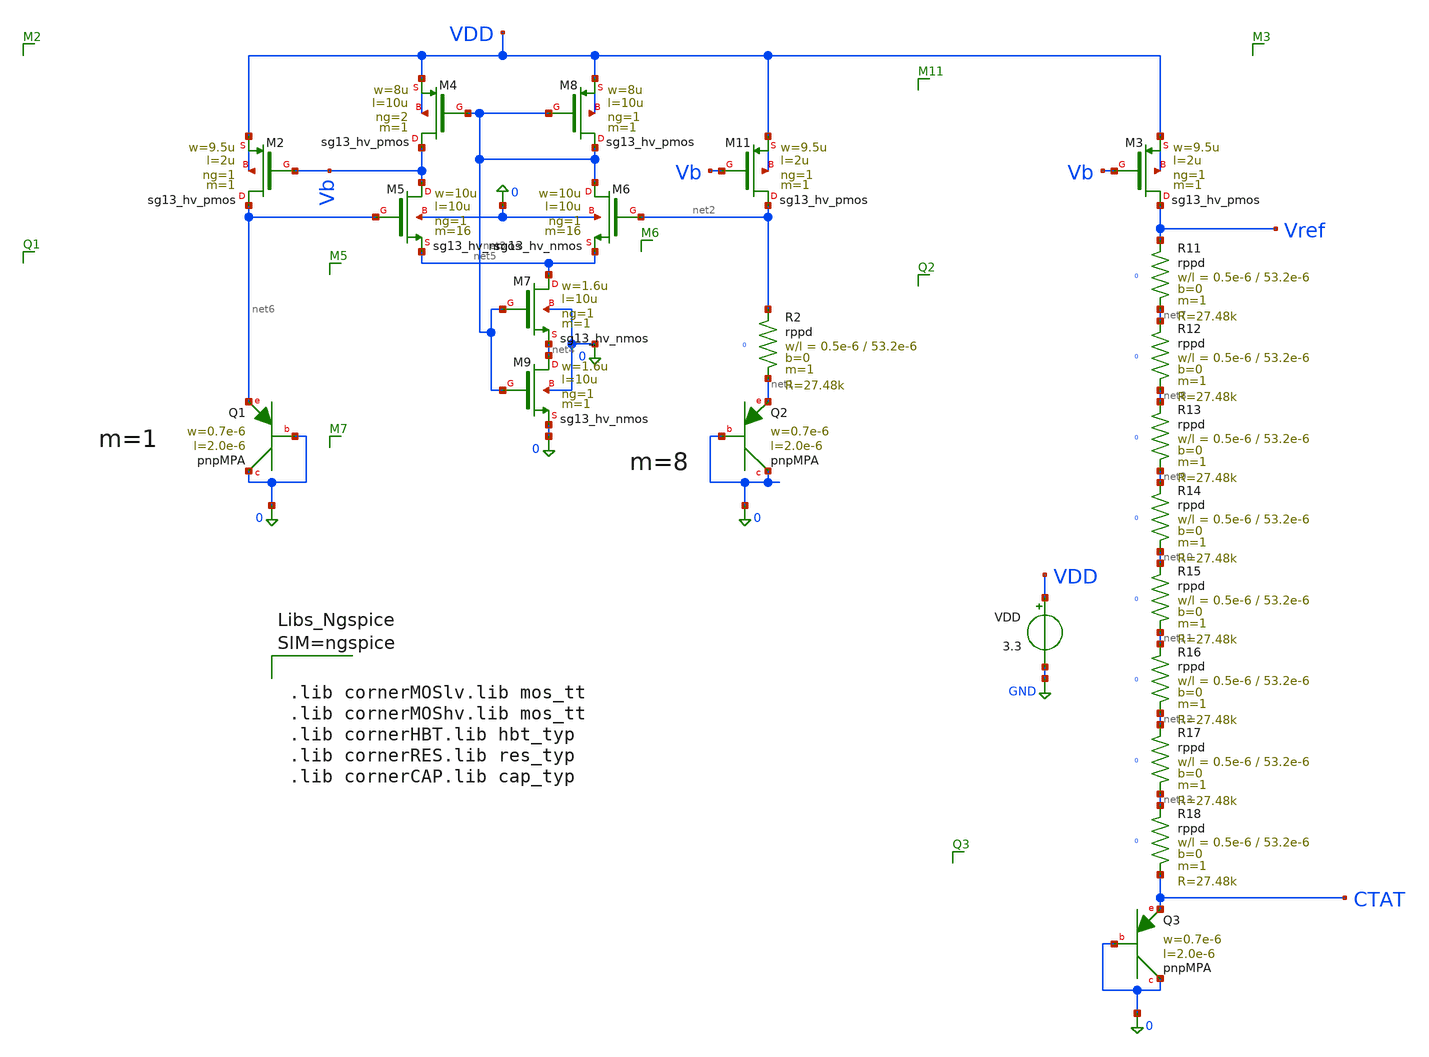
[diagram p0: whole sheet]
** sch_path: schematic/BGR1V2.sch
**.subckt BGR1V2
XQ1 0 0 net6 pnpMPA a=1.4p p=5.4u m=1
XQ2 0 0 net1 pnpMPA a=1.4p p=5.4u m=8
XQ3 0 0 CTAT pnpMPA a=1.4p p=5.4u m=1
XM2 net6 Vb VDD VDD sg13_hv_pmos w=9.5u l=2u ng=1 m=1 mm_ok=1
XM3 Vref Vb VDD VDD sg13_hv_pmos w=9.5u l=2u ng=1 m=1 mm_ok=1
VDD VDD GND 3.3
XM5 Vb net6 net5 0 sg13_hv_nmos w=10u l=10u ng=1 m=16 mm_ok=1
XM6 net3 net2 net5 0 sg13_hv_nmos w=10u l=10u ng=1 m=16 mm_ok=1
XM4 Vb net3 VDD VDD sg13_hv_pmos w=8u l=10u ng=2 m=1 mm_ok=1
XM8 net3 net3 VDD VDD sg13_hv_pmos w=8u l=10u ng=1 m=1 mm_ok=1
XM7 net5 net3 net4 0 sg13_hv_nmos w=1.6u l=10u ng=1 m=1 mm_ok=1
XR2 net2 net1 0 rppd w=0.5e-6 l=53.2e-6 m=1 b=0 mm_ok=1
XM9 net4 net3 0 0 sg13_hv_nmos w=1.6u l=10u ng=1 m=1 mm_ok=1
XM11 net2 Vb VDD VDD sg13_hv_pmos w=9.5u l=2u ng=1 m=1 mm_ok=1
XR11 Vref net7 0 rppd w=0.5e-6 l=53.2e-6 m=1 b=0 mm_ok=1
XR12 net7 net8 0 rppd w=0.5e-6 l=53.2e-6 m=1 b=0 mm_ok=1
XR13 net8 net9 0 rppd w=0.5e-6 l=53.2e-6 m=1 b=0 mm_ok=1
XR14 net9 net10 0 rppd w=0.5e-6 l=53.2e-6 m=1 b=0 mm_ok=1
XR15 net10 net11 0 rppd w=0.5e-6 l=53.2e-6 m=1 b=0 mm_ok=1
XR16 net11 net12 0 rppd w=0.5e-6 l=53.2e-6 m=1 b=0 mm_ok=1
XR17 net12 net13 0 rppd w=0.5e-6 l=53.2e-6 m=1 b=0 mm_ok=1
XR18 net13 CTAT 0 rppd w=0.5e-6 l=53.2e-6 m=1 b=0 mm_ok=1
**** begin user architecture code


.include BGR1V2.save
.control
save all

* ---------- Temperature sweep (VDD = 3.3 V) ----------
dc temp -40 125 1
let ptat = v(vref) - v(ctat)
let itot = -i(vdd)*1e6
let vmax = vecmax(v(vref))
let vmin = vecmin(v(vref))
let v27  = v(vref)[67]
let tc   = (vmax - vmin)/(v27*165)*1e6
let i27  = itot[67]
set v27s = $&v27
set tcs  = $&tc
set is   = $&i27
plot v(vref) title 'Vref vs Temperature' xlabel 'Temp [C]' ylabel 'Vref [V]'
plot v(vref) v(ctat) ptat title 'Vref = CTAT + PTAT term vs Temperature' xlabel 'Temp [C]' ylabel 'Voltage [V]'
plot itot    title 'Supply Current vs Temperature' xlabel 'Temp [C]' ylabel 'I [uA]'

* ---------- Supply sweep (27 C) ----------
option temp=27
dc VDD 0 3.6 0.05
let lr = (v(vref)[72] - v(vref)[50])/1.1/v(vref)[66]*100
set lrs = $&lr
plot v(vref) title 'Vref vs VDD' xlabel 'VDD [V]' ylabel 'Vref [V]'

* ---------- Vref vs VDD over temperature  ----------
dc VDD 0 3.6 0.05 temp 0 100 25
let ylo = $v27s - 0.01
let yhi = $v27s + 0.01
set ylos = $&ylo
set yhis = $&yhi
plot v(vref) xlimit 2.5 3.6 ylimit $ylos $yhis title 'Vref vs VDD, T = 0..100 C' xlabel 'VDD [V]' ylabel
+ 'Vref [V]'

* ---------- PSRR (27 C, VDD = 3.3 V) ----------
option temp=27
alter VDD ac=1
ac dec 10 1 1e9
let psrr = -db(v(vref))
let psrr100 = psrr[20]
set psrrs = $&psrr100
plot psrr title 'PSRR' xlabel 'Freq [Hz]' ylabel 'PSRR [dB]'

* ---------- Summary ----------
echo
echo ======== BANDGAP SUMMARY ========
echo Vref @ 27C            = $v27s V
echo TC (-40..125C)        = $tcs ppm/C
echo Supply current @ 27C  = $is uA
echo Line reg (2.5-3.6V)   = $lrs %/V
echo PSRR @ 100Hz          = $psrrs dB
echo =================================
.endc






.lib cornerMOSlv.lib mos_tt
.lib cornerMOShv.lib mos_tt
.lib cornerHBT.lib hbt_typ
.lib cornerRES.lib res_typ
.lib cornerCAP.lib cap_typ



**** end user architecture code
**.ends
.GLOBAL GND
.end
